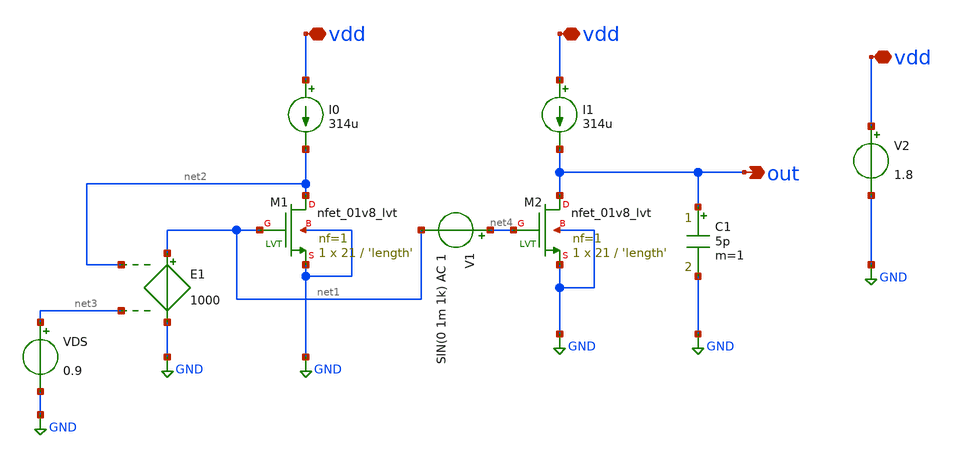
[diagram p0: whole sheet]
** sch_path: Simple-CS-Amplifier/csamp1.sch
**.subckt csamp1 vdd vdd vdd out
*.iopin vdd
*.iopin vdd
*.iopin vdd
*.opin out
XM1 net2 net1 GND GND sky130_fd_pr__nfet_01v8_lvt L='length' W=21 nf=1 ad='int((nf+1)/2) * W/nf * 0.29'
+ as='int((nf+2)/2) * W/nf * 0.29' pd='2*int((nf+1)/2) * (W/nf + 0.29)' ps='2*int((nf+2)/2) * (W/nf + 0.29)'
+ nrd='0.29 / W' nrs='0.29 / W' sa=0 sb=0 sd=0 mult=1 m=1
E1 net1 GND net2 net3 1000
I0 vdd net2 314u
VDS net3 GND 0.9
V2 vdd GND 1.8
XM2 out net4 GND GND sky130_fd_pr__nfet_01v8_lvt L='length' W=21 nf=1 ad='int((nf+1)/2) * W/nf * 0.29'
+ as='int((nf+2)/2) * W/nf * 0.29' pd='2*int((nf+1)/2) * (W/nf + 0.29)' ps='2*int((nf+2)/2) * (W/nf + 0.29)'
+ nrd='0.29 / W' nrs='0.29 / W' sa=0 sb=0 sd=0 mult=1 m=1
I1 vdd out 314u
V1 net4 net1 SIN(0 1m 1k) AC 1
C1 out GND 5p m=1
**** begin user architecture code



.lib /usr/local/share/pdk/sky130A/libs.tech/ngspice/sky130.lib.spice tt
.option wnflag=1 scale=1e-6
.param length = 0.30

.control
save all


save @m.xm1.msky130_fd_pr__nfet_01v8_lvt[vgs]
save @m.xm1.msky130_fd_pr__nfet_01v8_lvt[vds]


dc VDS 0.2 1.8 1m


let vgs = @m.xm1.msky130_fd_pr__nfet_01v8_lvt[vgs]
let vds = @m.xm1.msky130_fd_pr__nfet_01v8_lvt[vds]

let a = deriv(vgs)
let ao = -1/a

plot ao

*tran 10u 10m

*plot v(out)


*wrdata ao-L=0.40.txt ao
.endc


**** end user architecture code
**.ends
.GLOBAL GND
.end
